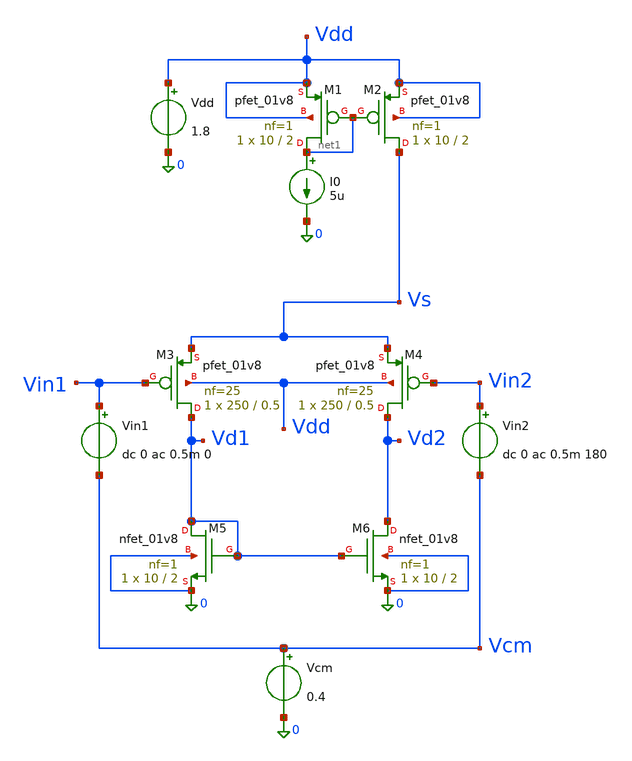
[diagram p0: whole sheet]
** sch_path: stage1/schematics/mirror_diffpair_activeload.sch
**.subckt mirror_diffpair_activeload
I0 net1 0 5u
XM1 net1 net1 Vdd Vdd sky130_fd_pr__pfet_01v8 L=2 W=10 nf=1 ad='int((1 + 1)/2) * 10 / 1 * 0.29' as='int((1 + 2)/2) * 10 / 1 * 0.29'
+ pd='2*int((1 + 1)/2) * (10 / 1 + 0.29)' ps='2*int((1 + 2)/2) * (10 / 1 + 0.29)' nrd='0.29 / 10 ' nrs='0.29 / 10 '
+ sa=0 sb=0 sd=0 mult=1 m=1
XM2 Vs net1 Vdd Vdd sky130_fd_pr__pfet_01v8 L=2 W=10 nf=1 ad='int((1 + 1)/2) * 10 / 1 * 0.29' as='int((1 + 2)/2) * 10 / 1 * 0.29'
+ pd='2*int((1 + 1)/2) * (10 / 1 + 0.29)' ps='2*int((1 + 2)/2) * (10 / 1 + 0.29)' nrd='0.29 / 10 ' nrs='0.29 / 10 '
+ sa=0 sb=0 sd=0 mult=1 m=1
Vdd Vdd 0 1.8
XM3 Vd1 Vin1 Vs Vdd sky130_fd_pr__pfet_01v8 L=0.5 W=250 nf=25 ad='int((25 + 1)/2) * 250 / 25 * 0.29'
+ as='int((25 + 2)/2) * 250 / 25 * 0.29' pd='2*int((25 + 1)/2) * (250 / 25 + 0.29)' ps='2*int((25 + 2)/2) * (250 / 25 + 0.29)'
+ nrd='0.29 / 250 ' nrs='0.29 / 250 ' sa=0 sb=0 sd=0 mult=1 m=1
XM4 Vd2 Vin2 Vs Vdd sky130_fd_pr__pfet_01v8 L=0.5 W=250 nf=25 ad='int((25 + 1)/2) * 250 / 25 * 0.29'
+ as='int((25 + 2)/2) * 250 / 25 * 0.29' pd='2*int((25 + 1)/2) * (250 / 25 + 0.29)' ps='2*int((25 + 2)/2) * (250 / 25 + 0.29)'
+ nrd='0.29 / 250 ' nrs='0.29 / 250 ' sa=0 sb=0 sd=0 mult=1 m=1
Vin1 Vin1 Vcm dc 0 ac 0.5m 0
XM5 Vd1 Vd1 0 0 sky130_fd_pr__nfet_01v8 L=2 W=10 nf=1 ad='int((1 + 1)/2) * 10 / 1 * 0.29' as='int((1 + 2)/2) * 10 / 1 * 0.29'
+ pd='2*int((1 + 1)/2) * (10 / 1 + 0.29)' ps='2*int((1 + 2)/2) * (10 / 1 + 0.29)' nrd='0.29 / 10 ' nrs='0.29 / 10 '
+ sa=0 sb=0 sd=0 mult=1 m=1
XM6 Vd2 Vd1 0 0 sky130_fd_pr__nfet_01v8 L=2 W=10 nf=1 ad='int((1 + 1)/2) * 10 / 1 * 0.29' as='int((1 + 2)/2) * 10 / 1 * 0.29'
+ pd='2*int((1 + 1)/2) * (10 / 1 + 0.29)' ps='2*int((1 + 2)/2) * (10 / 1 + 0.29)' nrd='0.29 / 10 ' nrs='0.29 / 10 '
+ sa=0 sb=0 sd=0 mult=1 m=1
Vin2 Vin2 Vcm dc 0 ac 0.5m 180
Vcm Vcm 0 0.4
**** begin user architecture code

** opencircuitdesign pdks install
.lib $::SKYWATER_MODELS/sky130.lib.spice tt


.include mirror_diffpair_activeload.save
.options savecurrents

.control
	save all
	ac dec 100 1 1G
	let H = v(Vd2) / (v(Vin1)-v(Vin2))
	let linear_differential_gain = mag(H)
	let phase = 180/PI*ph(H)
	let gain_db = db(H)

	plot gain_db
	plot phase
	plot linear_differential_gain

	meas ac gain_lf find gain_db at=1
	let gain_minus_3db = gain_lf - 3
	meas ac f3db when gain_db=$&gain_minus_3db fall=1

.endc

**** end user architecture code
**.ends
.end
